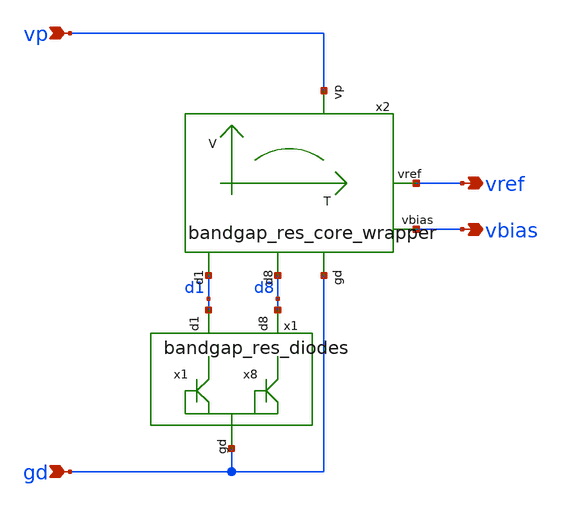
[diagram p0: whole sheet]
** sch_path: PLL0663-main/schematic/xschem/bandgap/bandgap_res_top.sch
**.subckt bandgap_res_top vp gd vref vbias
*.ipin vp
*.ipin gd
*.opin vref
*.opin vbias
x1 d1 d8 gd bandgap_res_diodes
x2 vp vref gd d8 d1 vbias bandgap_res_core_wrapper
**.ends
.end
